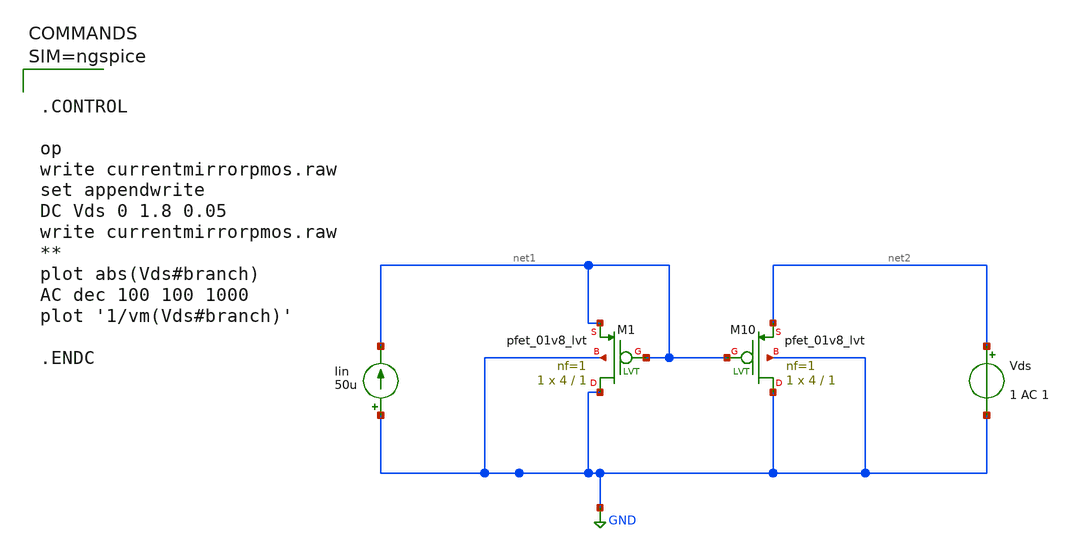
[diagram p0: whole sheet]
** sch_path: work/xschem/currentmirrorpmos.sch
**.subckt currentmirrorpmos
Iin GND net1 50u
Vds net2 GND 1 AC 1
XM10 GND net1 net2 GND sky130_fd_pr__pfet_01v8_lvt L=1 W=4 nf=1 ad='int((1 + 1)/2) * 4 / 1 * 0.29' as='int((1 + 2)/2) * 4 / 1 * 0.29'
+ pd='2*int((1 + 1)/2) * (4 / 1 + 0.29)' ps='2*int((1 + 2)/2) * (4 / 1 + 0.29)' nrd='0.29 / 4 ' nrs='0.29 / 4 '
+ sa=0 sb=0 sd=0 mult=1 m=1
XM1 GND net1 net1 GND sky130_fd_pr__pfet_01v8_lvt L=1 W=4 nf=1 ad='int((1 + 1)/2) * 4 / 1 * 0.29' as='int((1 + 2)/2) * 4 / 1 * 0.29'
+ pd='2*int((1 + 1)/2) * (4 / 1 + 0.29)' ps='2*int((1 + 2)/2) * (4 / 1 + 0.29)' nrd='0.29 / 4 ' nrs='0.29 / 4 '
+ sa=0 sb=0 sd=0 mult=1 m=1
**** begin user architecture code



.CONTROL

op
write currentmirrorpmos.raw
set appendwrite
DC Vds 0 1.8 0.05
write currentmirrorpmos.raw
**
plot abs(Vds#branch)
AC dec 100 100 1000
plot '1/vm(Vds#branch)'

.ENDC





** opencircuitdesign pdks install
.lib $::SKYWATER_MODELS/sky130.lib.spice tt

**** end user architecture code
**.ends
.GLOBAL GND
.end
